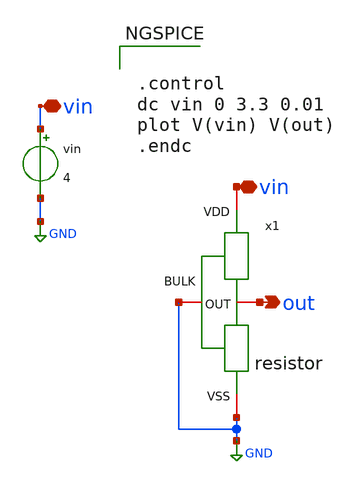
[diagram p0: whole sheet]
** sch_path: LDO/xschem/resistor/resistor-test.sch

.include $env(PDK_ROOT)/$env(PDK)/libs.tech/ngspice/design.ngspice
.lib $env(PDK_ROOT)/$env(PDK)/libs.tech/ngspice/sm141064.ngspice typical
.lib $env(PDK_ROOT)/$env(PDK)/libs.tech/ngspice/sm141064.ngspice mimcap_statistical
.lib $env(PDK_ROOT)/$env(PDK)/libs.tech/ngspice/sm141064.ngspice cap_mim
.lib $env(PDK_ROOT)/$env(PDK)/libs.tech/ngspice/sm141064.ngspice res_typical

**.subckt resistor-test out vin vin
*.opin out
*.iopin vin
*.iopin vin
vin vin GND 4
x1 vin GND out GND resistor
**** begin user architecture code

.control
dc vin 0 3.3 0.01
plot V(vin) V(out)
.endc

**** end user architecture code
**.ends

* expanding   symbol:  resistor.sym # of pins=4
** sym_path: LDO/xschem/resistor/resistor.sym
** sch_path: LDO/xschem/resistor/resistor.sch
.subckt resistor VDD BULK OUT VSS
*.iopin OUT
*.iopin VSS
*.iopin VDD
*.iopin BULK
XR1 OUT VDD BULK ppolyf_u_1k r_width=1e-6 r_length=20e-6 m=10
XR2 VSS OUT BULK ppolyf_u_1k r_width=1e-6 r_length=20e-6 m=6
.ends

.GLOBAL GND
.end
